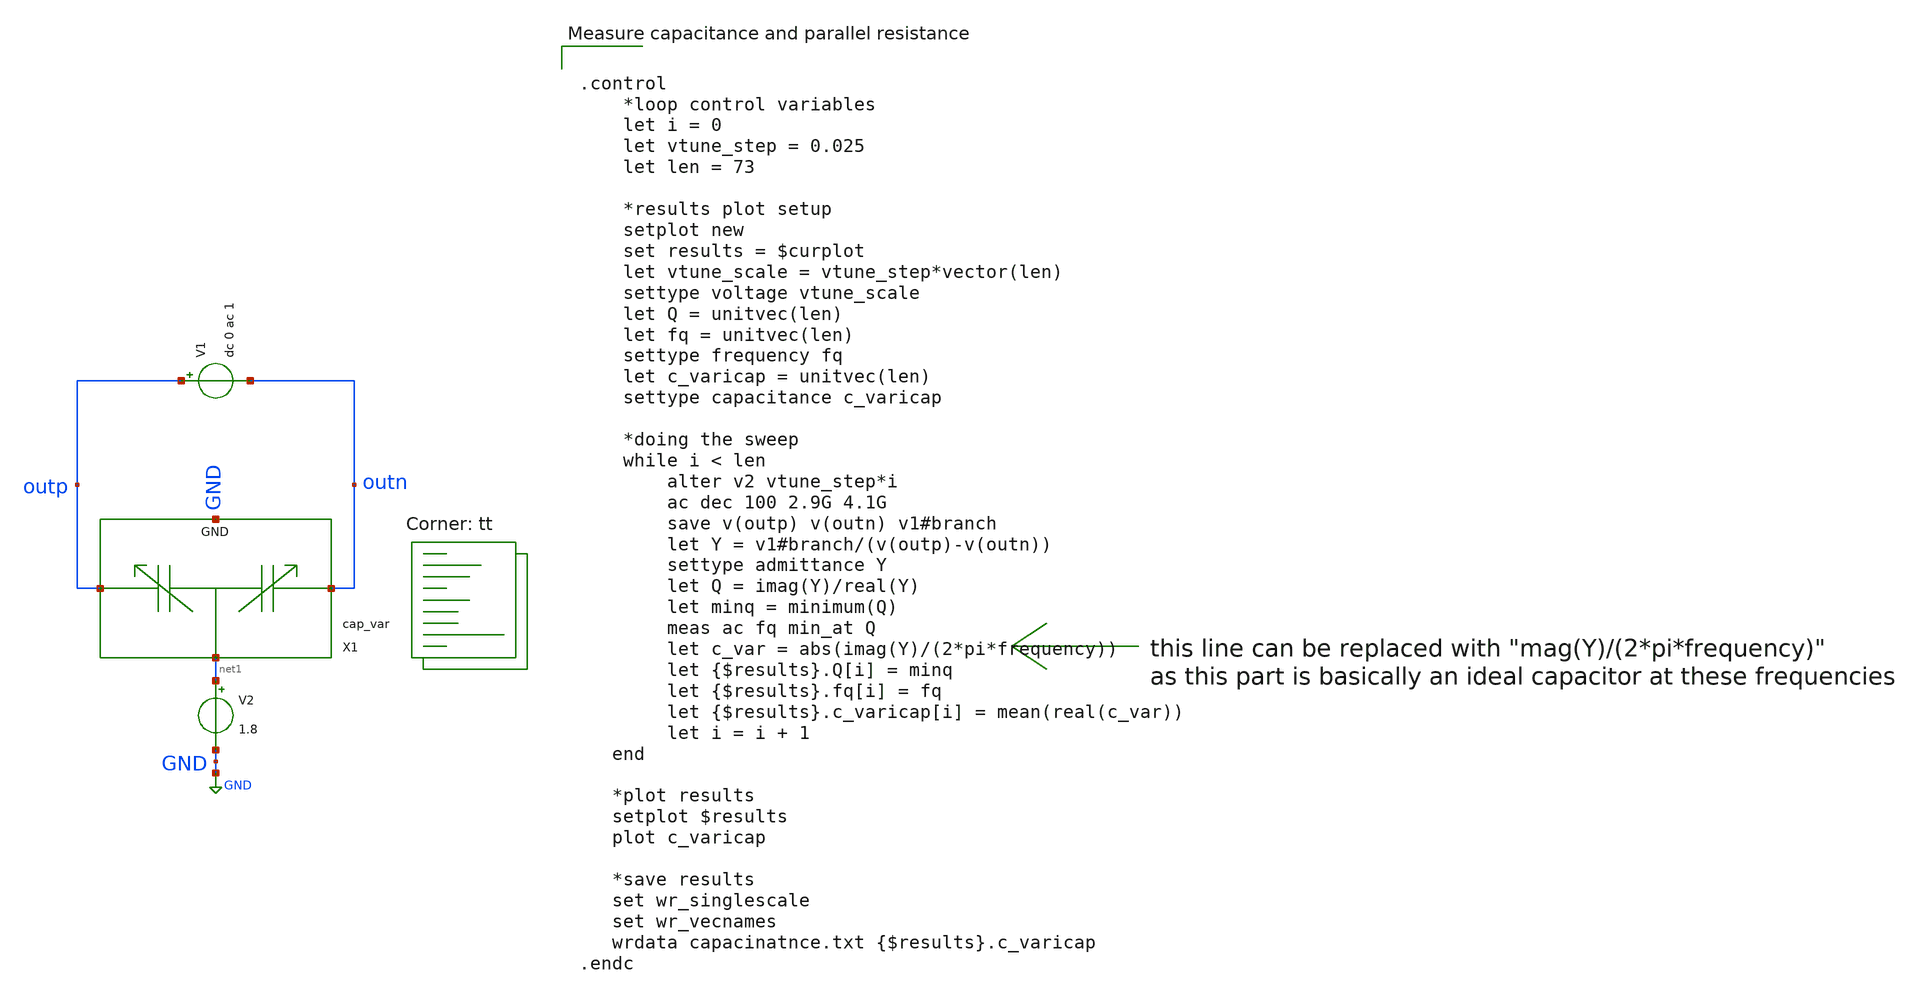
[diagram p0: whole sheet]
** sch_path: xschem/vco/testbenches/varicap/varicap_capacity_measurement_tb.sch
**.subckt varicap_capacity_measurement_tb
X1 outp outn GND net1 cap_var
V1 outp outn dc 0 ac 1
V2 net1 GND 1.8
**** begin user architecture code
.lib $::SKYWATER_MODELS/sky130.lib.spice tt


.control
    *loop control variables
    let i = 0
    let vtune_step = 0.025
    let len = 73

    *results plot setup
    setplot new
    set results = $curplot
    let vtune_scale = vtune_step*vector(len)
    settype voltage vtune_scale
    let Q = unitvec(len)
    let fq = unitvec(len)
    settype frequency fq
    let c_varicap = unitvec(len)
    settype capacitance c_varicap

    *doing the sweep
    while i < len
        alter v2 vtune_step*i
        ac dec 100 2.9G 4.1G
        save v(outp) v(outn) v1#branch
        let Y = v1#branch/(v(outp)-v(outn))
        settype admittance Y
        let Q = imag(Y)/real(Y)
        let minq = minimum(Q)
        meas ac fq min_at Q
        let c_var = abs(imag(Y)/(2*pi*frequency))
        let {$results}.Q[i] = minq
        let {$results}.fq[i] = fq
        let {$results}.c_varicap[i] = mean(real(c_var))
        let i = i + 1
   end

   *plot results
   setplot $results
   plot c_varicap

   *save results
   set wr_singlescale
   set wr_vecnames
   wrdata capacinatnce.txt {$results}.c_varicap
.endc


**** end user architecture code
**.ends

* expanding   symbol:  vco/parts/cap_var.sym # of pins=4
** sym_path: xschem/vco/parts/cap_var.sym
** sch_path: xschem/vco/parts/cap_var.sch
.subckt cap_var OUT_P OUT_N GND Vtune
*.iopin OUT_P
*.iopin OUT_N
*.iopin GND
*.ipin Vtune
XC1 OUT_P Vtune GND sky130_fd_pr__cap_var_lvt W=4 L=0.6 VM=14 m=14
XC2 OUT_N Vtune GND sky130_fd_pr__cap_var_lvt W=4 L=0.6 VM=14 m=14
.ends

.GLOBAL GND
.end
